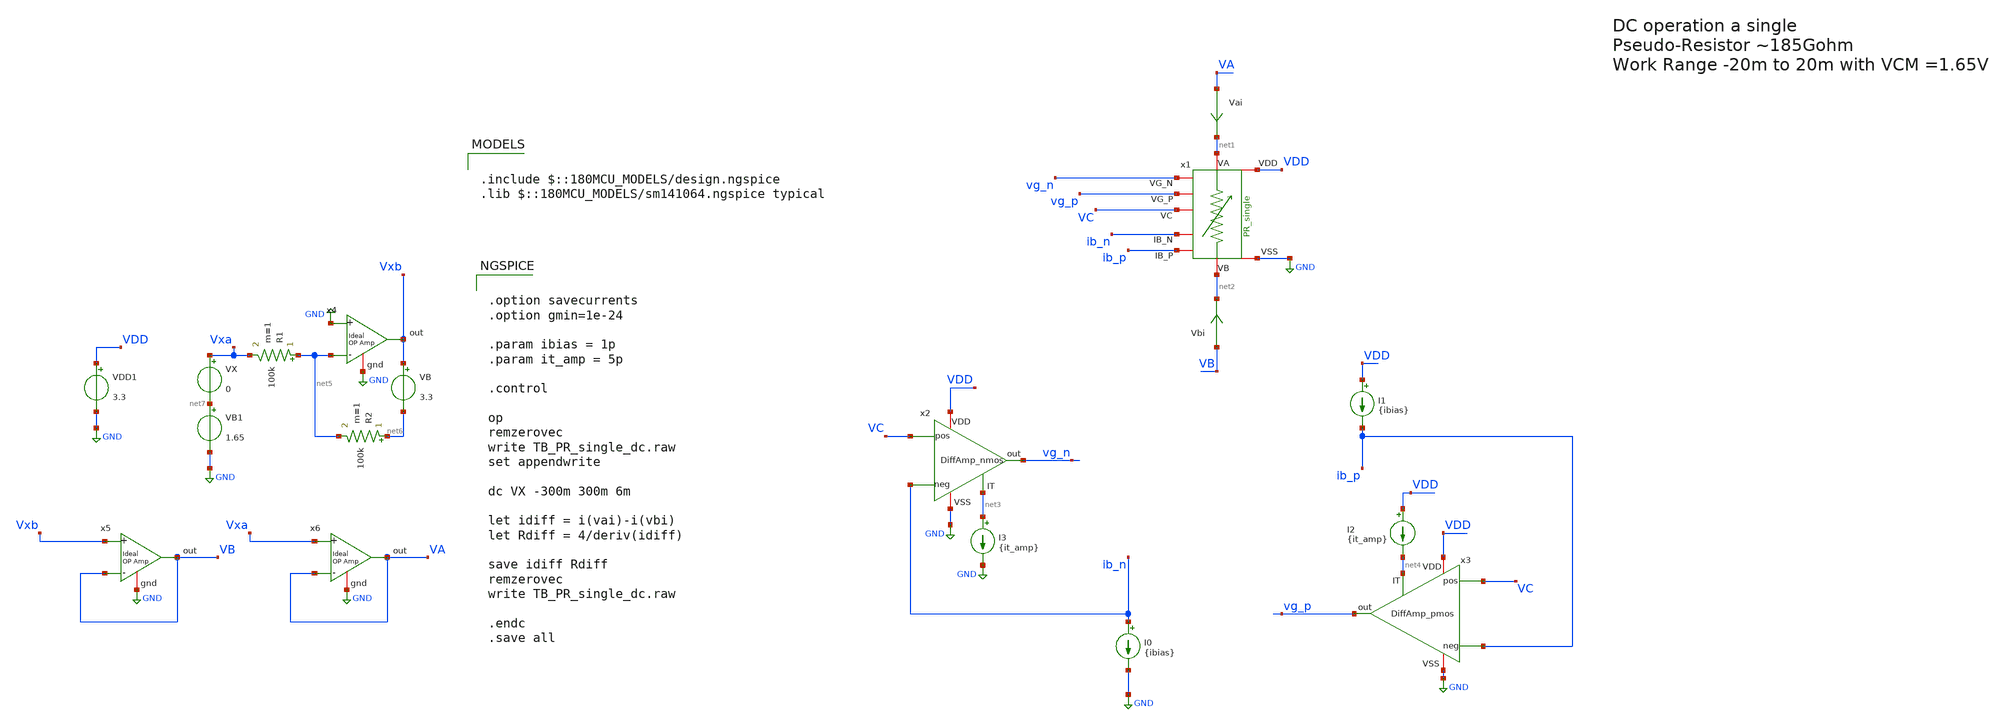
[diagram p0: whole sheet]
** sch_path: TIA/xschem/PseudoResistor/TB_PR_single_dc.sch
**.subckt TB_PR_single_dc
I0 ib_n GND {ibias}
I1 VDD ib_p {ibias}
VDD1 VDD GND 3.3
Vai VA net1 0
.save i(vai)
Vbi VB net2 0
.save i(vbi)
x2 VDD GND VC ib_n net3 vg_n DiffAmp_nmos
I2 VDD net4 {it_amp}
x3 VDD GND net4 ib_p VC vg_p DiffAmp_pmos
I3 net3 GND {it_amp}
x1 net1 net2 vg_n vg_p ib_n ib_p VDD GND VC PR_single
VX Vxa net7 0
VB Vxb net6 3.3
R1 net5 Vxa 100k m=1
R2 net6 net5 100k m=1
VB1 net7 GND 1.65
x4 Vxb GND net5 GND ampOp_ideal
x5 VB Vxb VB GND ampOp_ideal
x6 VA Vxa VA GND ampOp_ideal
**** begin user architecture code

.include $::180MCU_MODELS/design.ngspice
.lib $::180MCU_MODELS/sm141064.ngspice typical



.option savecurrents
.option gmin=1e-24

.param ibias = 1p
.param it_amp = 5p

.control

op
remzerovec
write TB_PR_single_dc.raw
set appendwrite

dc VX -300m 300m 6m

let idiff = i(vai)-i(vbi)
let Rdiff = 4/deriv(idiff)

save idiff Rdiff
remzerovec
write TB_PR_single_dc.raw

.endc
.save all


**** end user architecture code
**.ends
.GLOBAL GND
.end
